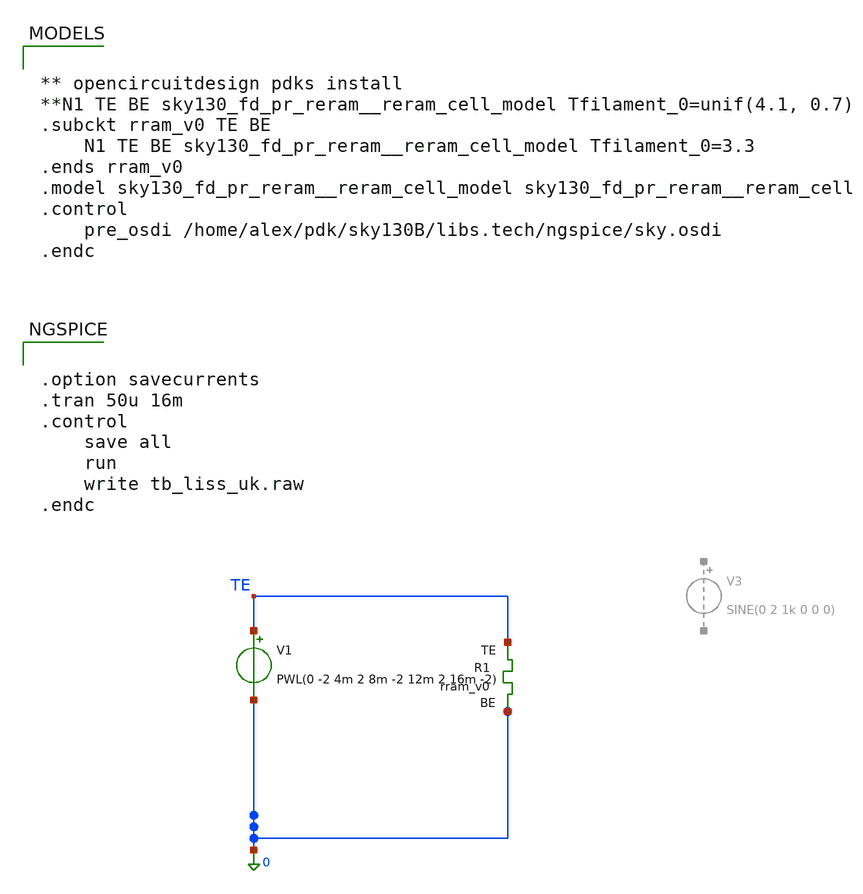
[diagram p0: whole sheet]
** sch_path: memristor_models/rram_london/tb_liss_uk.sch
**.subckt tb_liss_uk
XR1 TE 0 rram_v0
V1 TE 0 PWL(0 -2 4m 2 8m -2 12m 2 16m -2)
**** begin user architecture code

** opencircuitdesign pdks install
**N1 TE BE sky130_fd_pr_reram__reram_cell_model Tfilament_0=unif(4.1, 0.7)
.subckt rram_v0 TE BE
	N1 TE BE sky130_fd_pr_reram__reram_cell_model Tfilament_0=3.3
.ends rram_v0
.model sky130_fd_pr_reram__reram_cell_model sky130_fd_pr_reram__reram_cell
.control
	pre_osdi /home/alex/pdk/sky130B/libs.tech/ngspice/sky.osdi
.endc



.option savecurrents
.tran 50u 16m
.control
	save all
	run
	write tb_liss_uk.raw
.endc



**** end user architecture code
**.ends
.end
